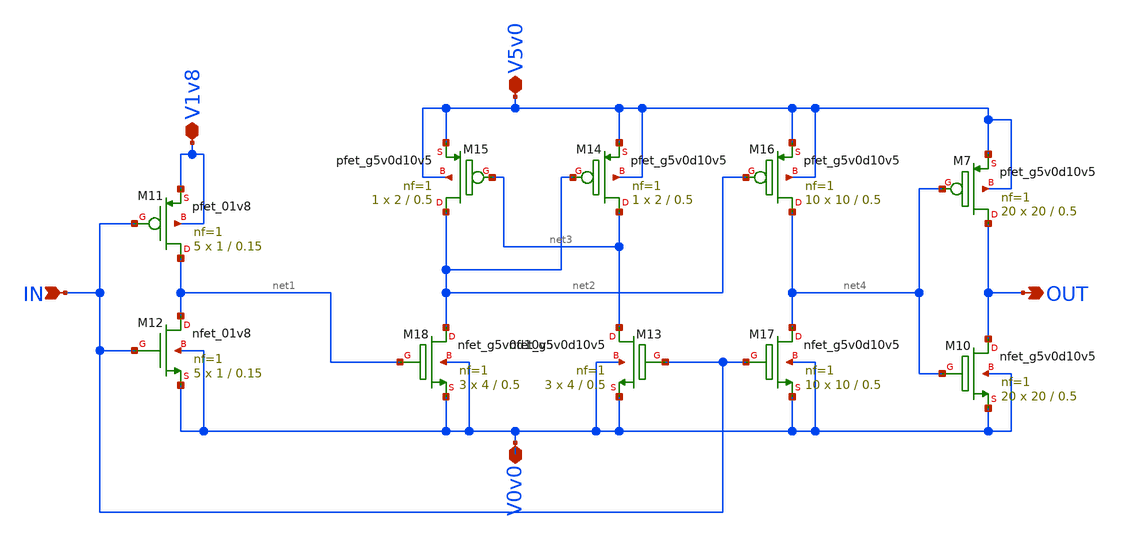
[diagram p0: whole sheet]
** sch_path: xschem/level_shifter.sch
**.subckt level_shifter IN V1v8 V5v0 OUT V0v0
*.ipin IN
*.iopin V1v8
*.iopin V5v0
*.opin OUT
*.iopin V0v0
XM11 net1 IN V1v8 V1v8 sky130_fd_pr__pfet_01v8 L=0.15 W=1 nf=1 ad='int((nf+1)/2) * W/nf * 0.29' as='int((nf+2)/2) * W/nf * 0.29'
+ pd='2*int((nf+1)/2) * (W/nf + 0.29)' ps='2*int((nf+2)/2) * (W/nf + 0.29)' nrd='0.29 / W' nrs='0.29 / W'
+ sa=0 sb=0 sd=0 mult=5 m=5
XM12 net1 IN V0v0 V0v0 sky130_fd_pr__nfet_01v8 L=0.15 W=1 nf=1 ad='int((nf+1)/2) * W/nf * 0.29' as='int((nf+2)/2) * W/nf * 0.29'
+ pd='2*int((nf+1)/2) * (W/nf + 0.29)' ps='2*int((nf+2)/2) * (W/nf + 0.29)' nrd='0.29 / W' nrs='0.29 / W'
+ sa=0 sb=0 sd=0 mult=5 m=5
XM15 net2 net3 V5v0 V5v0 sky130_fd_pr__pfet_g5v0d10v5 L=0.5 W=2 nf=1 ad='int((nf+1)/2) * W/nf * 0.29'
+ as='int((nf+2)/2) * W/nf * 0.29' pd='2*int((nf+1)/2) * (W/nf + 0.29)' ps='2*int((nf+2)/2) * (W/nf + 0.29)'
+ nrd='0.29 / W' nrs='0.29 / W' sa=0 sb=0 sd=0 mult=1 m=1
XM14 net3 net2 V5v0 V5v0 sky130_fd_pr__pfet_g5v0d10v5 L=0.5 W=2 nf=1 ad='int((nf+1)/2) * W/nf * 0.29'
+ as='int((nf+2)/2) * W/nf * 0.29' pd='2*int((nf+1)/2) * (W/nf + 0.29)' ps='2*int((nf+2)/2) * (W/nf + 0.29)'
+ nrd='0.29 / W' nrs='0.29 / W' sa=0 sb=0 sd=0 mult=1 m=1
XM16 net4 net2 V5v0 V5v0 sky130_fd_pr__pfet_g5v0d10v5 L=0.5 W=10 nf=1 ad='int((nf+1)/2) * W/nf * 0.29'
+ as='int((nf+2)/2) * W/nf * 0.29' pd='2*int((nf+1)/2) * (W/nf + 0.29)' ps='2*int((nf+2)/2) * (W/nf + 0.29)'
+ nrd='0.29 / W' nrs='0.29 / W' sa=0 sb=0 sd=0 mult=10 m=10
XM18 net2 net1 V0v0 V0v0 sky130_fd_pr__nfet_g5v0d10v5 L=0.5 W=4 nf=1 ad='int((nf+1)/2) * W/nf * 0.29'
+ as='int((nf+2)/2) * W/nf * 0.29' pd='2*int((nf+1)/2) * (W/nf + 0.29)' ps='2*int((nf+2)/2) * (W/nf + 0.29)'
+ nrd='0.29 / W' nrs='0.29 / W' sa=0 sb=0 sd=0 mult=3 m=3
XM13 net3 IN V0v0 V0v0 sky130_fd_pr__nfet_g5v0d10v5 L=0.5 W=4 nf=1 ad='int((nf+1)/2) * W/nf * 0.29' as='int((nf+2)/2) * W/nf * 0.29'
+ pd='2*int((nf+1)/2) * (W/nf + 0.29)' ps='2*int((nf+2)/2) * (W/nf + 0.29)' nrd='0.29 / W' nrs='0.29 / W'
+ sa=0 sb=0 sd=0 mult=3 m=3
XM17 net4 IN V0v0 V0v0 sky130_fd_pr__nfet_g5v0d10v5 L=0.5 W=10 nf=1 ad='int((nf+1)/2) * W/nf * 0.29'
+ as='int((nf+2)/2) * W/nf * 0.29' pd='2*int((nf+1)/2) * (W/nf + 0.29)' ps='2*int((nf+2)/2) * (W/nf + 0.29)'
+ nrd='0.29 / W' nrs='0.29 / W' sa=0 sb=0 sd=0 mult=10 m=10
XM7 OUT net4 V5v0 V5v0 sky130_fd_pr__pfet_g5v0d10v5 L=0.5 W=20 nf=1 ad='int((nf+1)/2) * W/nf * 0.29'
+ as='int((nf+2)/2) * W/nf * 0.29' pd='2*int((nf+1)/2) * (W/nf + 0.29)' ps='2*int((nf+2)/2) * (W/nf + 0.29)'
+ nrd='0.29 / W' nrs='0.29 / W' sa=0 sb=0 sd=0 mult=20 m=20
XM10 OUT net4 V0v0 V0v0 sky130_fd_pr__nfet_g5v0d10v5 L=0.5 W=20 nf=1 ad='int((nf+1)/2) * W/nf * 0.29'
+ as='int((nf+2)/2) * W/nf * 0.29' pd='2*int((nf+1)/2) * (W/nf + 0.29)' ps='2*int((nf+2)/2) * (W/nf + 0.29)'
+ nrd='0.29 / W' nrs='0.29 / W' sa=0 sb=0 sd=0 mult=20 m=20
**.ends
.end
